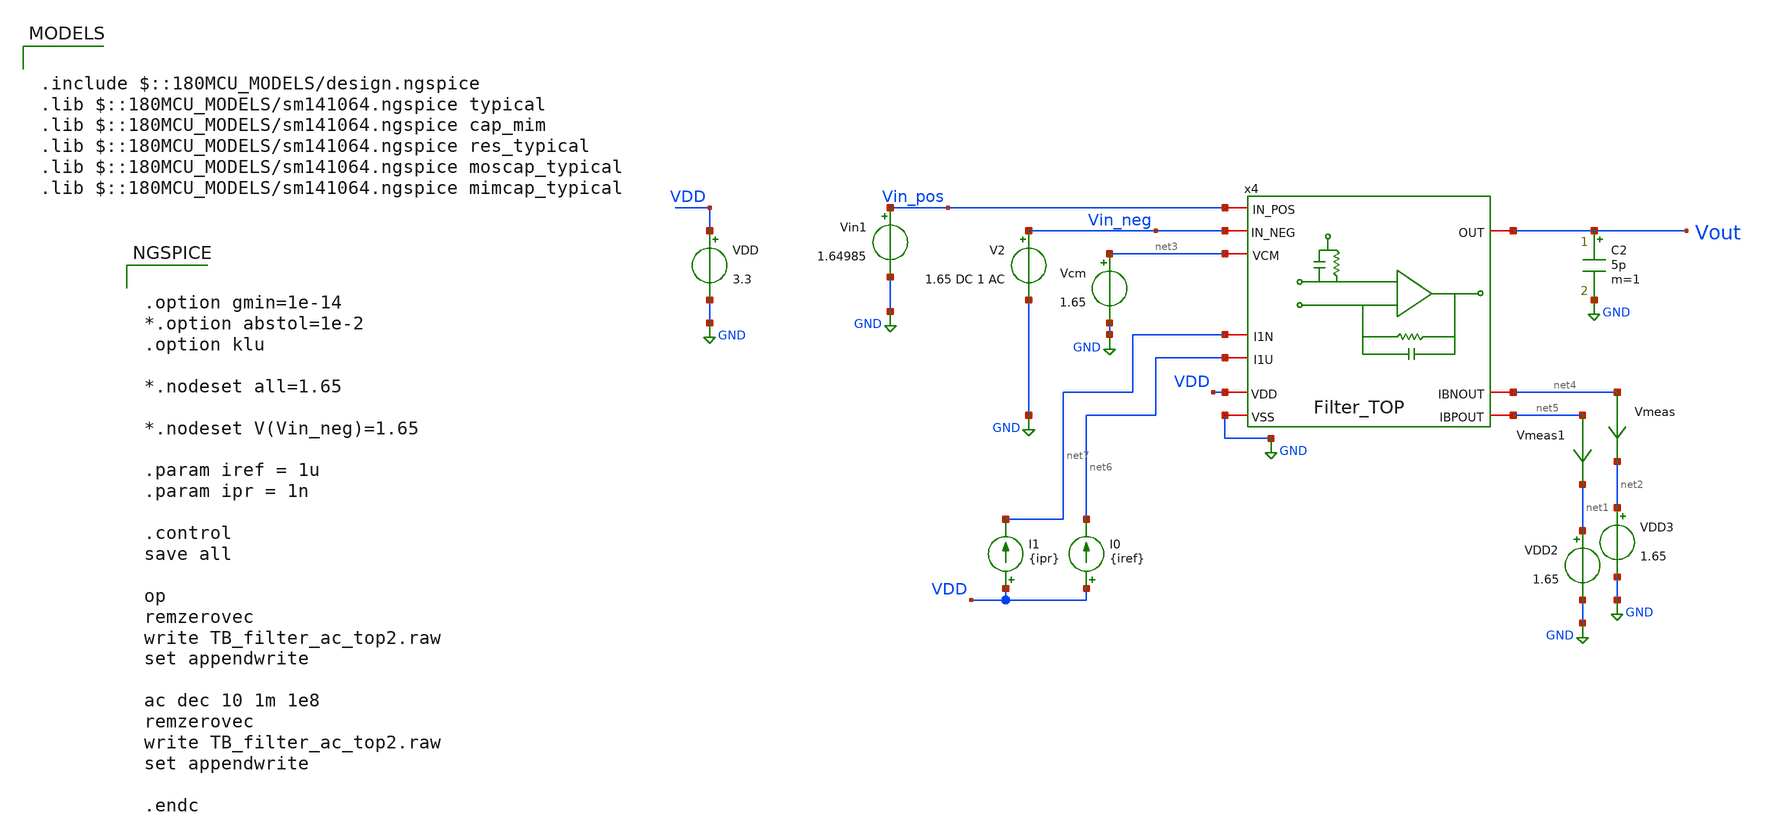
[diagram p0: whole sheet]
** sch_path: TIA_Filter/TB_filter_ac_top2.sch
**.subckt TB_filter_ac_top2
VDD VDD GND 3.3
C2 Vout GND 5p m=1
Vin1 Vin_pos GND 1.64985
V2 Vin_neg GND 1.65 DC 1 AC
I0 VDD net6 {iref}
I1 VDD net7 {ipr}
Vmeas net4 net2 0
.save i(vmeas)
Vmeas1 net5 net1 0
.save i(vmeas1)
Vcm net3 GND 1.65
VDD2 net1 GND 1.65
VDD3 net2 GND 1.65
x4 Vin_pos Vin_neg net3 Vout VDD GND net7 net6 net4 net5 Filter_TOP
**** begin user architecture code

.include $::180MCU_MODELS/design.ngspice
.lib $::180MCU_MODELS/sm141064.ngspice typical
.lib $::180MCU_MODELS/sm141064.ngspice cap_mim
.lib $::180MCU_MODELS/sm141064.ngspice res_typical
.lib $::180MCU_MODELS/sm141064.ngspice moscap_typical
.lib $::180MCU_MODELS/sm141064.ngspice mimcap_typical



.option gmin=1e-14
*.option abstol=1e-2
.option klu

*.nodeset all=1.65

*.nodeset V(Vin_neg)=1.65

.param iref = 1u
.param ipr = 1n

.control
save all

op
remzerovec
write TB_filter_ac_top2.raw
set appendwrite

ac dec 10 1m 1e8
remzerovec
write TB_filter_ac_top2.raw
set appendwrite

.endc


**** end user architecture code
**.ends
.GLOBAL GND
.end
